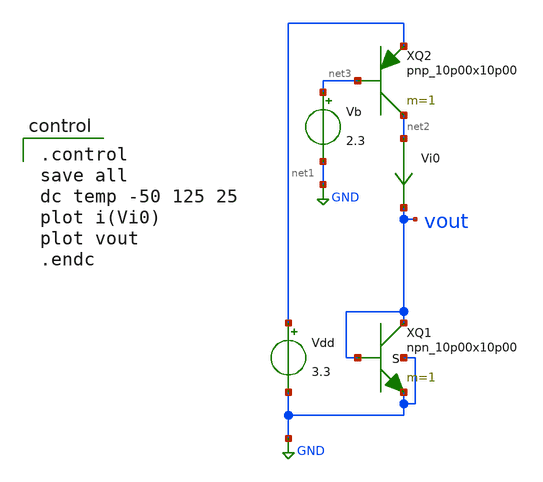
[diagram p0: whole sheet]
** sch_path: bgr/npn-diode-ctat.sch
**.subckt npn-diode-ctat
XQ1 vout vout GND GND npn_10p00x10p00 m=1
Vdd net1 GND 3.3
Vi0 net2 vout 0
.save i(vi0)
XQ2 net2 net3 net1 pnp_10p00x10p00 m=1
Vb net3 GND 2.3
**** begin user architecture code

.include $::180MCU_MODELS/design.ngspice
.lib $::180MCU_MODELS/sm141064.ngspice typical
.lib $::180MCU_MODELS/sm141064.ngspice res_typical
.lib $::180MCU_MODELS/sm141064.ngspice moscap_typical
.lib $::180MCU_MODELS/sm141064.ngspice bjt_typical
* .lib $::180MCU_MODELS/sm141064.ngspice res_statistical


.control
save all
dc temp -50 125 25
plot i(Vi0)
plot vout
.endc

**** end user architecture code
**.ends
.GLOBAL GND
.end
